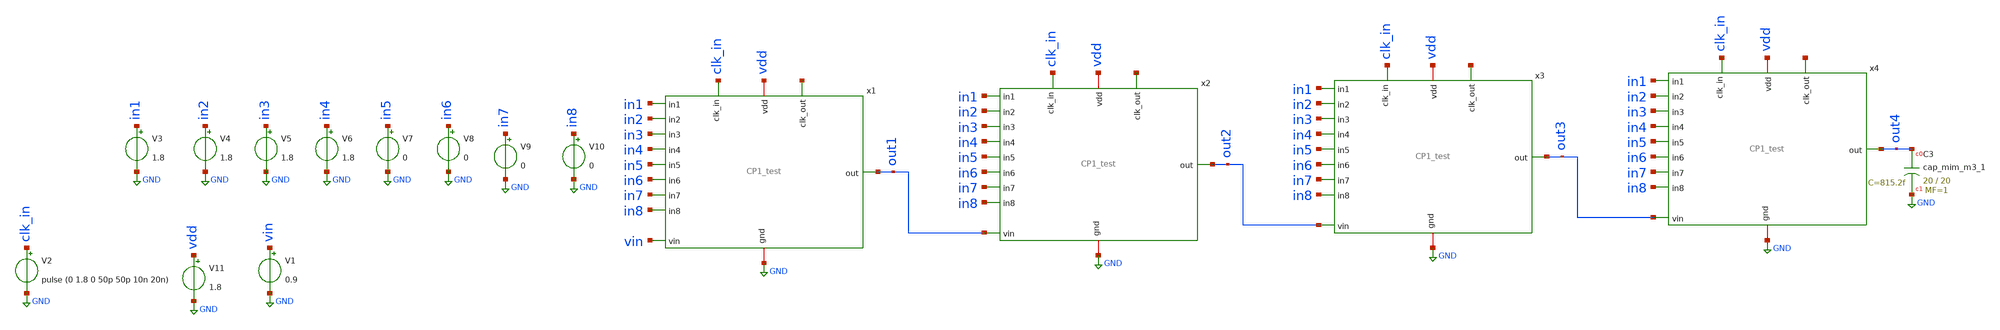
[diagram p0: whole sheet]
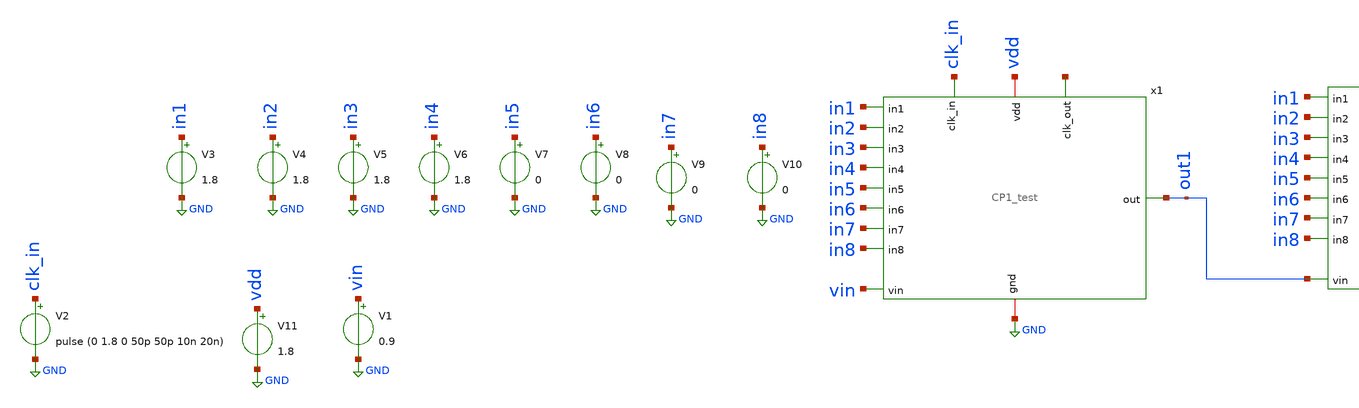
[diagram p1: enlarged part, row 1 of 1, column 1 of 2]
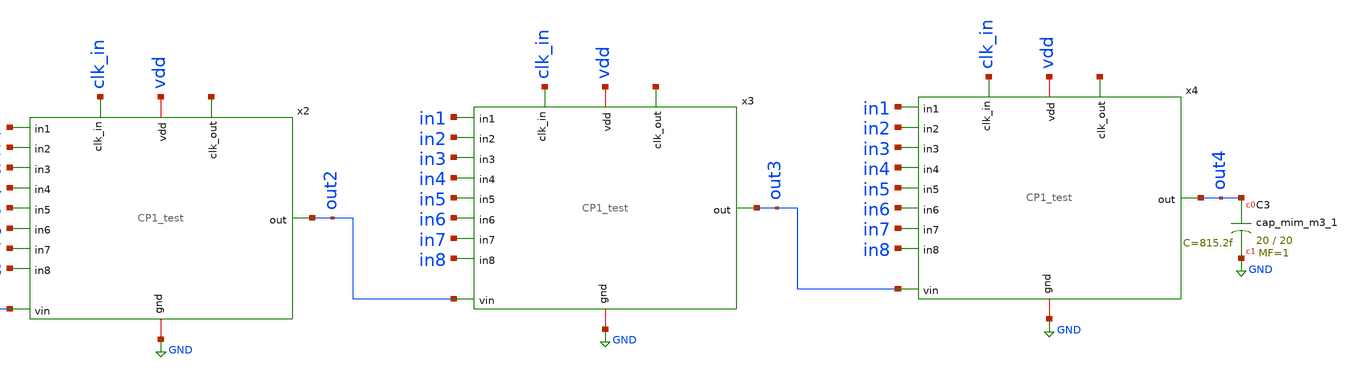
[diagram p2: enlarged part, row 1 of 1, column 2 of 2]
** sch_path: xschem/CP1_tb.sch
**.subckt CP1_tb
V1 vin GND 0.9
V2 clk_in GND pulse (0 1.8 0 50p 50p 10n 20n)
V3 in1 GND 1.8
V4 in2 GND 1.8
V5 in3 GND 1.8
V6 in4 GND 1.8
V7 in5 GND 0
V8 in6 GND 0
V9 in7 GND 0
V10 in8 GND 0
V11 vdd GND 1.8
x1 GND clk_in vin out1 in1 in2 in3 in4 in5 in6 in7 in8 vdd net1 CP1_test
x2 GND clk_in out1 out2 in1 in2 in3 in4 in5 in6 in7 in8 vdd net2 CP1_test
x3 GND clk_in out2 out3 in1 in2 in3 in4 in5 in6 in7 in8 vdd net3 CP1_test
x4 GND clk_in out3 out4 in1 in2 in3 in4 in5 in6 in7 in8 vdd net4 CP1_test
XC3 out4 GND sky130_fd_pr__cap_mim_m3_1 W=20 L=20 MF=1 m=1
**** begin user architecture code

** opencircuitdesign pdks install
.lib $::SKYWATER_MODELS/sky130.lib.spice tt




.tran 100n 5u
.save all


**** end user architecture code
**.ends
.GLOBAL GND
.end
